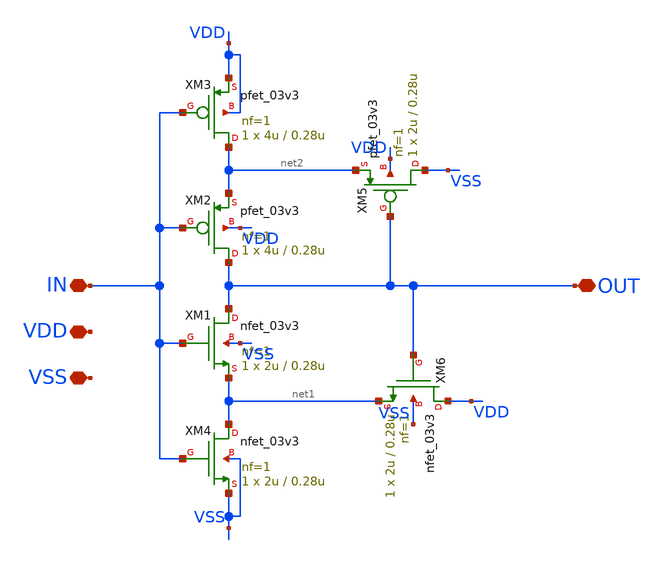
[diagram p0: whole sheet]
** sch_path: designs/libs/qw_core_analog/schmitt_trigger.sch
**.subckt schmitt_trigger OUT IN VDD VSS
*.iopin OUT
*.iopin IN
*.iopin VDD
*.iopin VSS
XM1 OUT IN net1 VSS nfet_03v3 L=0.28u W=2u nf=1 ad='int((nf+1)/2) * W/nf * 0.18u' as='int((nf+2)/2) * W/nf * 0.18u'
+ pd='2*int((nf+1)/2) * (W/nf + 0.18u)' ps='2*int((nf+2)/2) * (W/nf + 0.18u)' nrd='0.18u / W' nrs='0.18u / W'
+ sa=0 sb=0 sd=0 m=1
XM2 OUT IN net2 VDD pfet_03v3 L=0.28u W=4u nf=1 ad='int((nf+1)/2) * W/nf * 0.18u' as='int((nf+2)/2) * W/nf * 0.18u'
+ pd='2*int((nf+1)/2) * (W/nf + 0.18u)' ps='2*int((nf+2)/2) * (W/nf + 0.18u)' nrd='0.18u / W' nrs='0.18u / W'
+ sa=0 sb=0 sd=0 m=1
XM3 net2 IN VDD VDD pfet_03v3 L=0.28u W=4u nf=1 ad='int((nf+1)/2) * W/nf * 0.18u' as='int((nf+2)/2) * W/nf * 0.18u'
+ pd='2*int((nf+1)/2) * (W/nf + 0.18u)' ps='2*int((nf+2)/2) * (W/nf + 0.18u)' nrd='0.18u / W' nrs='0.18u / W'
+ sa=0 sb=0 sd=0 m=1
XM4 net1 IN VSS VSS nfet_03v3 L=0.28u W=2u nf=1 ad='int((nf+1)/2) * W/nf * 0.18u' as='int((nf+2)/2) * W/nf * 0.18u'
+ pd='2*int((nf+1)/2) * (W/nf + 0.18u)' ps='2*int((nf+2)/2) * (W/nf + 0.18u)' nrd='0.18u / W' nrs='0.18u / W'
+ sa=0 sb=0 sd=0 m=1
XM5 VSS OUT net2 VDD pfet_03v3 L=0.28u W=2u nf=1 ad='int((nf+1)/2) * W/nf * 0.18u' as='int((nf+2)/2) * W/nf * 0.18u'
+ pd='2*int((nf+1)/2) * (W/nf + 0.18u)' ps='2*int((nf+2)/2) * (W/nf + 0.18u)' nrd='0.18u / W' nrs='0.18u / W'
+ sa=0 sb=0 sd=0 m=1
XM6 VDD OUT net1 VSS nfet_03v3 L=0.28u W=2u nf=1 ad='int((nf+1)/2) * W/nf * 0.18u' as='int((nf+2)/2) * W/nf * 0.18u'
+ pd='2*int((nf+1)/2) * (W/nf + 0.18u)' ps='2*int((nf+2)/2) * (W/nf + 0.18u)' nrd='0.18u / W' nrs='0.18u / W'
+ sa=0 sb=0 sd=0 m=1
**.ends
.end
